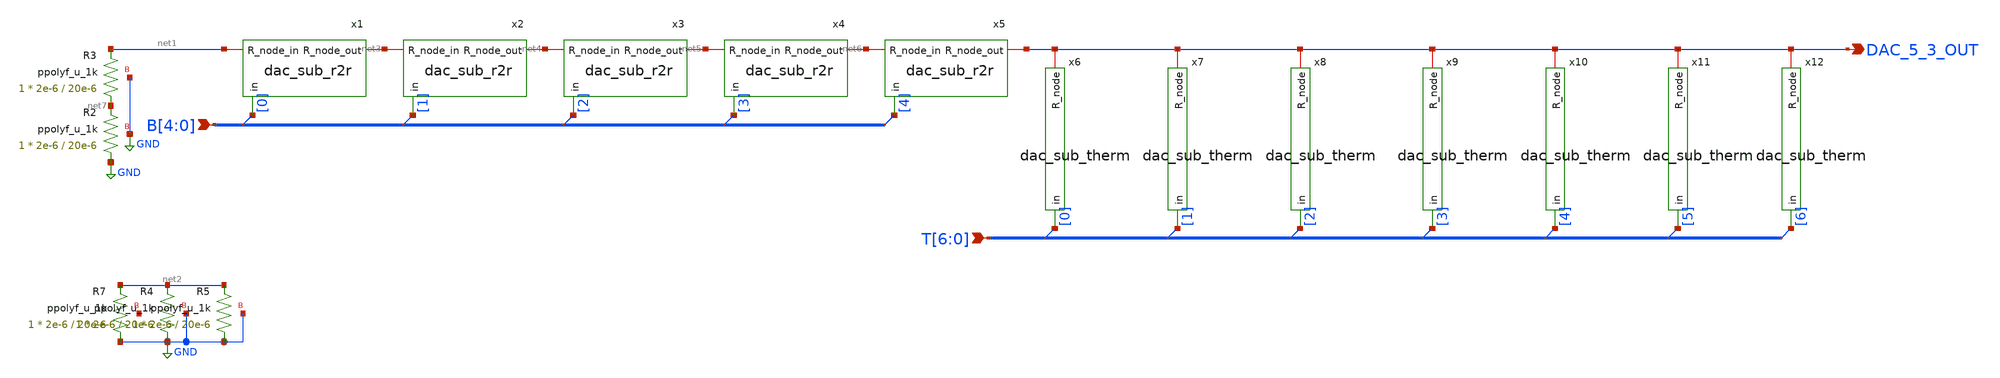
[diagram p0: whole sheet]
** sch_path: xschem/dac_5_3.sch
**.subckt dac_5_3 B[4],B[3],B[2],B[1],B[0] T[6],T[5],T[4],T[3],T[2],T[1],T[0] DAC_5_3_OUT
*.ipin B[4],B[3],B[2],B[1],B[0]
*.ipin T[6],T[5],T[4],T[3],T[2],T[1],T[0]
*.opin DAC_5_3_OUT
x1 net3 net1 B[0] dac_sub_r2r
x2 net4 net3 B[1] dac_sub_r2r
x3 net5 net4 B[2] dac_sub_r2r
x4 net6 net5 B[3] dac_sub_r2r
x5 DAC_5_3_OUT net6 B[4] dac_sub_r2r
* tap: B[4:0] --> B[0]
* tap: B[4:0] --> B[1]
* tap: B[4:0] --> B[2]
* tap: B[4:0] --> B[3]
* tap: B[4:0] --> B[4]
x6 DAC_5_3_OUT T[0] dac_sub_therm
x7 DAC_5_3_OUT T[1] dac_sub_therm
x8 DAC_5_3_OUT T[2] dac_sub_therm
x9 DAC_5_3_OUT T[3] dac_sub_therm
x10 DAC_5_3_OUT T[4] dac_sub_therm
x11 DAC_5_3_OUT T[5] dac_sub_therm
x12 DAC_5_3_OUT T[6] dac_sub_therm
* tap: T[6:0] --> T[0]
* tap: T[6:0] --> T[1]
* tap: T[6:0] --> T[2]
* tap: T[6:0] --> T[3]
* tap: T[6:0] --> T[4]
* tap: T[6:0] --> T[5]
* tap: T[6:0] --> T[6]
XR2 GND net7 GND ppolyf_u_1k r_width=2e-6 r_length=20e-6 m=1
XR3 net7 net1 GND ppolyf_u_1k r_width=2e-6 r_length=20e-6 m=1
XR4 GND net2 GND ppolyf_u_1k r_width=2e-6 r_length=20e-6 m=1
XR5 GND net2 GND ppolyf_u_1k r_width=2e-6 r_length=20e-6 m=1
XR7 GND net2 net8 ppolyf_u_1k r_width=2e-6 r_length=20e-6 m=1
**.ends

* expanding   symbol:  dac_sub_r2r.sym # of pins=3
** sym_path: xschem/dac_sub_r2r.sym
** sch_path: xschem/dac_sub_r2r.sch
.subckt dac_sub_r2r R_node_out R_node_in in
*.ipin in
*.iopin R_node_out
*.iopin R_node_in
XR7 in net1 GND ppolyf_u_1k r_width=2e-6 r_length=20e-6 m=1
XR1 net1 R_node_in GND ppolyf_u_1k r_width=2e-6 r_length=20e-6 m=1
XR2 net2 R_node_in GND ppolyf_u_1k r_width=2e-6 r_length=20e-6 m=1
XR3 R_node_out net2 GND ppolyf_u_1k r_width=2e-6 r_length=20e-6 m=1
XR4 net3 R_node_in GND ppolyf_u_1k r_width=2e-6 r_length=20e-6 m=1
XR5 R_node_out net3 GND ppolyf_u_1k r_width=2e-6 r_length=20e-6 m=1
.ends


* expanding   symbol:  dac_sub_therm.sym # of pins=2
** sym_path: xschem/dac_sub_therm.sym
** sch_path: xschem/dac_sub_therm.sch
.subckt dac_sub_therm R_node in
*.ipin in
*.iopin R_node
XR7 in net1 GND ppolyf_u_1k r_width=2e-6 r_length=20e-6 m=1
XR1 net1 R_node GND ppolyf_u_1k r_width=2e-6 r_length=20e-6 m=1
.ends

.GLOBAL GND
.end
